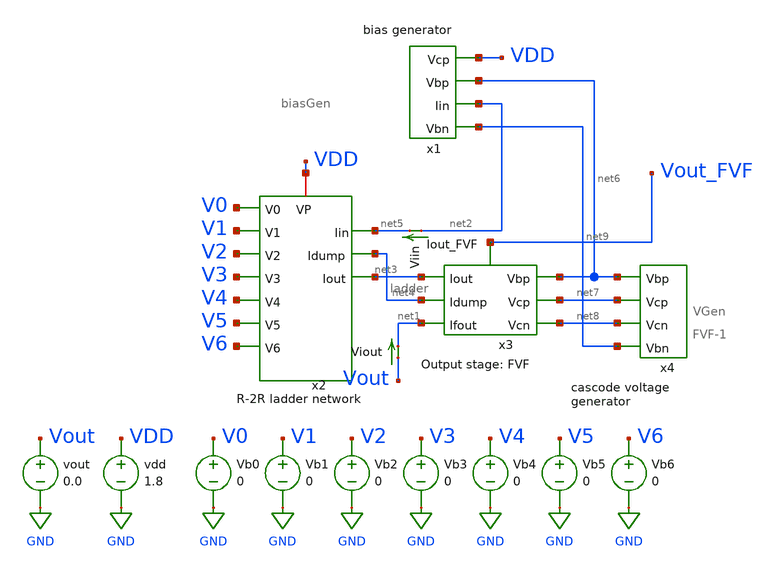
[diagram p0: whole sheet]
** sch_path: xschem/mp4_dac_simulation_mc.sch
**.subckt mp4_dac_simulation_mc
Vb1 V1 GND 0
Vb2 V2 GND 0
Vb3 V3 GND 0
Vb4 V4 GND 0
Vb5 V5 GND 0
Vb6 V6 GND 0
Vb0 V0 GND 0
vdd VDD GND 1.8
vout Vout GND 0.0
Viout Vout net1 0
.save i(viout)
Viin net2 net5 0
.save i(viin)
x2 V0 VDD net4 net3 net5 V1 V2 V3 V4 V5 V6 ladder
x1 net6 net2 net9 VDD biasGen
x3 net6 net7 net3 net8 net1 net4 Vout_FVF FVF-1
x4 net6 net8 net7 net9 VGen
**** begin user architecture code

.option wnflag=1
.param MC_SWITCH=1.0
.lib ~/skywater/skywater-pdk/libraries/sky130_fd_pr_ngspice/latest/models/sky130.lib.spice tt



.control
  set wr_singlescale
  let runs = 10
  let run = 1
  while run <= runs
  set appendwrite = FALSE
  set wr_vecnames
  let code = 0
   while code < 128
    if code eq 0
      let b0 = 0
    else
      let b0 = code % 2
    end
    if floor(code / 2) eq 0
      let b1 = 0
    else
      let b1 = floor(code / 2) % 2
    end
    if floor(code / 4) eq 0
      let b2 = 0
    else
      let b2 = floor(code / 4) % 2
    end
    if floor(code / 8) eq 0
      let b3 = 0
    else
      let b3 = floor(code / 8) % 2
    end
    if floor(code / 16) eq 0
      let b4 = 0
    else
      let b4 = floor(code / 16) % 2
    end
    if floor(code / 32) eq 0
      let b5 = 0
    else
      let b5 = floor(code / 32) % 2
    end
    if floor(code / 64) eq 0
      let b6 = 0
    else
      let b6 = floor(code / 64) % 2
    end
    alter Vb0 1.8*$&b0
    alter Vb1 1.8*$&b1
    alter Vb2 1.8*$&b2
    alter Vb3 1.8*$&b3
    alter Vb4 1.8*$&b4
    alter Vb5 1.8*$&b5
    alter Vb6 1.8*$&b6
    save all
    op
    wrdata ~/Documents/DAC-VLSI/simulation_results/mc/dac_simulation_mc_vout05_{$&run}.txt v(b0) v(b1)
+ v(b2) v(b3) v(b4) v(b5) v(b6) v(Vout_FVF) v(vout) i(Viin) i(Viout)
    if code eq 0
      set appendwrite
      set wr_vecnames = FALSE
    end
    let code = code + 1
  end
  reset
  let run = run + 1
  end
  quit
.endc


**** end user architecture code
**.ends
.GLOBAL GND
.end
